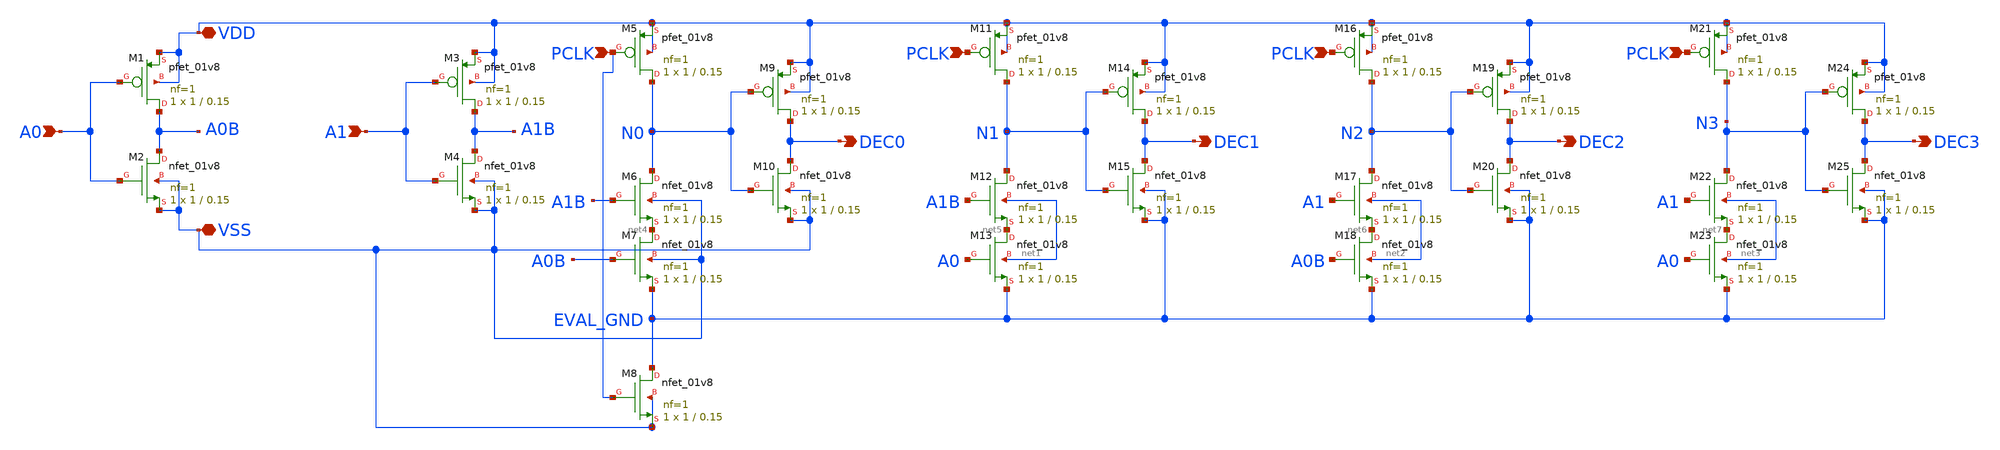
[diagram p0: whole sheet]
** sch_path: cells/row_decoder/row_decoder.sch
**.subckt row_decoder VDD VSS A0 A1 PCLK DEC0 PCLK DEC1 PCLK DEC2 PCLK DEC3
*.iopin VDD
*.iopin VSS
*.ipin A0
*.ipin A1
*.ipin PCLK
*.opin DEC0
*.ipin PCLK
*.opin DEC1
*.ipin PCLK
*.opin DEC2
*.ipin PCLK
*.opin DEC3
XM1 A0B A0 VDD VDD sky130_fd_pr__pfet_01v8 L=0.15 W=1 nf=1 ad='int((nf+1)/2) * W/nf * 0.29' as='int((nf+2)/2) * W/nf * 0.29'
+ pd='2*int((nf+1)/2) * (W/nf + 0.29)' ps='2*int((nf+2)/2) * (W/nf + 0.29)' nrd='0.29 / W' nrs='0.29 / W'
+ sa=0 sb=0 sd=0 mult=1 m=1
XM2 A0B A0 VSS VSS sky130_fd_pr__nfet_01v8 L=0.15 W=1 nf=1 ad='int((nf+1)/2) * W/nf * 0.29' as='int((nf+2)/2) * W/nf * 0.29'
+ pd='2*int((nf+1)/2) * (W/nf + 0.29)' ps='2*int((nf+2)/2) * (W/nf + 0.29)' nrd='0.29 / W' nrs='0.29 / W'
+ sa=0 sb=0 sd=0 mult=1 m=1
XM3 A1B A1 VDD VDD sky130_fd_pr__pfet_01v8 L=0.15 W=1 nf=1 ad='int((nf+1)/2) * W/nf * 0.29' as='int((nf+2)/2) * W/nf * 0.29'
+ pd='2*int((nf+1)/2) * (W/nf + 0.29)' ps='2*int((nf+2)/2) * (W/nf + 0.29)' nrd='0.29 / W' nrs='0.29 / W'
+ sa=0 sb=0 sd=0 mult=1 m=1
XM4 A1B A1 VSS VSS sky130_fd_pr__nfet_01v8 L=0.15 W=1 nf=1 ad='int((nf+1)/2) * W/nf * 0.29' as='int((nf+2)/2) * W/nf * 0.29'
+ pd='2*int((nf+1)/2) * (W/nf + 0.29)' ps='2*int((nf+2)/2) * (W/nf + 0.29)' nrd='0.29 / W' nrs='0.29 / W'
+ sa=0 sb=0 sd=0 mult=1 m=1
XM5 N0 PCLK VDD VDD sky130_fd_pr__pfet_01v8 L=0.15 W=1 nf=1 ad='int((nf+1)/2) * W/nf * 0.29' as='int((nf+2)/2) * W/nf * 0.29'
+ pd='2*int((nf+1)/2) * (W/nf + 0.29)' ps='2*int((nf+2)/2) * (W/nf + 0.29)' nrd='0.29 / W' nrs='0.29 / W'
+ sa=0 sb=0 sd=0 mult=1 m=1
XM6 N0 A1B net4 VSS sky130_fd_pr__nfet_01v8 L=0.15 W=1 nf=1 ad='int((nf+1)/2) * W/nf * 0.29' as='int((nf+2)/2) * W/nf * 0.29'
+ pd='2*int((nf+1)/2) * (W/nf + 0.29)' ps='2*int((nf+2)/2) * (W/nf + 0.29)' nrd='0.29 / W' nrs='0.29 / W'
+ sa=0 sb=0 sd=0 mult=1 m=1
XM7 net4 A0B EVAL_GND VSS sky130_fd_pr__nfet_01v8 L=0.15 W=1 nf=1 ad='int((nf+1)/2) * W/nf * 0.29' as='int((nf+2)/2) * W/nf * 0.29'
+ pd='2*int((nf+1)/2) * (W/nf + 0.29)' ps='2*int((nf+2)/2) * (W/nf + 0.29)' nrd='0.29 / W' nrs='0.29 / W'
+ sa=0 sb=0 sd=0 mult=1 m=1
XM8 EVAL_GND PCLK VSS VSS sky130_fd_pr__nfet_01v8 L=0.15 W=1 nf=1 ad='int((nf+1)/2) * W/nf * 0.29' as='int((nf+2)/2) * W/nf * 0.29'
+ pd='2*int((nf+1)/2) * (W/nf + 0.29)' ps='2*int((nf+2)/2) * (W/nf + 0.29)' nrd='0.29 / W' nrs='0.29 / W'
+ sa=0 sb=0 sd=0 mult=1 m=1
XM9 DEC0 N0 VDD VDD sky130_fd_pr__pfet_01v8 L=0.15 W=1 nf=1 ad='int((nf+1)/2) * W/nf * 0.29' as='int((nf+2)/2) * W/nf * 0.29'
+ pd='2*int((nf+1)/2) * (W/nf + 0.29)' ps='2*int((nf+2)/2) * (W/nf + 0.29)' nrd='0.29 / W' nrs='0.29 / W'
+ sa=0 sb=0 sd=0 mult=1 m=1
XM10 DEC0 N0 VSS VSS sky130_fd_pr__nfet_01v8 L=0.15 W=1 nf=1 ad='int((nf+1)/2) * W/nf * 0.29' as='int((nf+2)/2) * W/nf * 0.29'
+ pd='2*int((nf+1)/2) * (W/nf + 0.29)' ps='2*int((nf+2)/2) * (W/nf + 0.29)' nrd='0.29 / W' nrs='0.29 / W'
+ sa=0 sb=0 sd=0 mult=1 m=1
XM11 N1 PCLK VDD VDD sky130_fd_pr__pfet_01v8 L=0.15 W=1 nf=1 ad='int((nf+1)/2) * W/nf * 0.29' as='int((nf+2)/2) * W/nf * 0.29'
+ pd='2*int((nf+1)/2) * (W/nf + 0.29)' ps='2*int((nf+2)/2) * (W/nf + 0.29)' nrd='0.29 / W' nrs='0.29 / W'
+ sa=0 sb=0 sd=0 mult=1 m=1
XM12 N1 A1B net5 net1 sky130_fd_pr__nfet_01v8 L=0.15 W=1 nf=1 ad='int((nf+1)/2) * W/nf * 0.29' as='int((nf+2)/2) * W/nf * 0.29'
+ pd='2*int((nf+1)/2) * (W/nf + 0.29)' ps='2*int((nf+2)/2) * (W/nf + 0.29)' nrd='0.29 / W' nrs='0.29 / W'
+ sa=0 sb=0 sd=0 mult=1 m=1
XM13 net5 A0 EVAL_GND net1 sky130_fd_pr__nfet_01v8 L=0.15 W=1 nf=1 ad='int((nf+1)/2) * W/nf * 0.29' as='int((nf+2)/2) * W/nf * 0.29'
+ pd='2*int((nf+1)/2) * (W/nf + 0.29)' ps='2*int((nf+2)/2) * (W/nf + 0.29)' nrd='0.29 / W' nrs='0.29 / W'
+ sa=0 sb=0 sd=0 mult=1 m=1
XM14 DEC1 N1 VDD VDD sky130_fd_pr__pfet_01v8 L=0.15 W=1 nf=1 ad='int((nf+1)/2) * W/nf * 0.29' as='int((nf+2)/2) * W/nf * 0.29'
+ pd='2*int((nf+1)/2) * (W/nf + 0.29)' ps='2*int((nf+2)/2) * (W/nf + 0.29)' nrd='0.29 / W' nrs='0.29 / W'
+ sa=0 sb=0 sd=0 mult=1 m=1
XM15 DEC1 N1 EVAL_GND EVAL_GND sky130_fd_pr__nfet_01v8 L=0.15 W=1 nf=1 ad='int((nf+1)/2) * W/nf * 0.29'
+ as='int((nf+2)/2) * W/nf * 0.29' pd='2*int((nf+1)/2) * (W/nf + 0.29)' ps='2*int((nf+2)/2) * (W/nf + 0.29)'
+ nrd='0.29 / W' nrs='0.29 / W' sa=0 sb=0 sd=0 mult=1 m=1
XM16 N2 PCLK VDD VDD sky130_fd_pr__pfet_01v8 L=0.15 W=1 nf=1 ad='int((nf+1)/2) * W/nf * 0.29' as='int((nf+2)/2) * W/nf * 0.29'
+ pd='2*int((nf+1)/2) * (W/nf + 0.29)' ps='2*int((nf+2)/2) * (W/nf + 0.29)' nrd='0.29 / W' nrs='0.29 / W'
+ sa=0 sb=0 sd=0 mult=1 m=1
XM17 N2 A1 net6 net2 sky130_fd_pr__nfet_01v8 L=0.15 W=1 nf=1 ad='int((nf+1)/2) * W/nf * 0.29' as='int((nf+2)/2) * W/nf * 0.29'
+ pd='2*int((nf+1)/2) * (W/nf + 0.29)' ps='2*int((nf+2)/2) * (W/nf + 0.29)' nrd='0.29 / W' nrs='0.29 / W'
+ sa=0 sb=0 sd=0 mult=1 m=1
XM18 net6 A0B EVAL_GND net2 sky130_fd_pr__nfet_01v8 L=0.15 W=1 nf=1 ad='int((nf+1)/2) * W/nf * 0.29'
+ as='int((nf+2)/2) * W/nf * 0.29' pd='2*int((nf+1)/2) * (W/nf + 0.29)' ps='2*int((nf+2)/2) * (W/nf + 0.29)'
+ nrd='0.29 / W' nrs='0.29 / W' sa=0 sb=0 sd=0 mult=1 m=1
XM19 DEC2 N2 VDD VDD sky130_fd_pr__pfet_01v8 L=0.15 W=1 nf=1 ad='int((nf+1)/2) * W/nf * 0.29' as='int((nf+2)/2) * W/nf * 0.29'
+ pd='2*int((nf+1)/2) * (W/nf + 0.29)' ps='2*int((nf+2)/2) * (W/nf + 0.29)' nrd='0.29 / W' nrs='0.29 / W'
+ sa=0 sb=0 sd=0 mult=1 m=1
XM20 DEC2 N2 EVAL_GND EVAL_GND sky130_fd_pr__nfet_01v8 L=0.15 W=1 nf=1 ad='int((nf+1)/2) * W/nf * 0.29'
+ as='int((nf+2)/2) * W/nf * 0.29' pd='2*int((nf+1)/2) * (W/nf + 0.29)' ps='2*int((nf+2)/2) * (W/nf + 0.29)'
+ nrd='0.29 / W' nrs='0.29 / W' sa=0 sb=0 sd=0 mult=1 m=1
XM21 N3 PCLK VDD VDD sky130_fd_pr__pfet_01v8 L=0.15 W=1 nf=1 ad='int((nf+1)/2) * W/nf * 0.29' as='int((nf+2)/2) * W/nf * 0.29'
+ pd='2*int((nf+1)/2) * (W/nf + 0.29)' ps='2*int((nf+2)/2) * (W/nf + 0.29)' nrd='0.29 / W' nrs='0.29 / W'
+ sa=0 sb=0 sd=0 mult=1 m=1
XM22 N3 A1 net7 net3 sky130_fd_pr__nfet_01v8 L=0.15 W=1 nf=1 ad='int((nf+1)/2) * W/nf * 0.29' as='int((nf+2)/2) * W/nf * 0.29'
+ pd='2*int((nf+1)/2) * (W/nf + 0.29)' ps='2*int((nf+2)/2) * (W/nf + 0.29)' nrd='0.29 / W' nrs='0.29 / W'
+ sa=0 sb=0 sd=0 mult=1 m=1
XM23 net7 A0 EVAL_GND net3 sky130_fd_pr__nfet_01v8 L=0.15 W=1 nf=1 ad='int((nf+1)/2) * W/nf * 0.29' as='int((nf+2)/2) * W/nf * 0.29'
+ pd='2*int((nf+1)/2) * (W/nf + 0.29)' ps='2*int((nf+2)/2) * (W/nf + 0.29)' nrd='0.29 / W' nrs='0.29 / W'
+ sa=0 sb=0 sd=0 mult=1 m=1
XM24 DEC3 N3 VDD VDD sky130_fd_pr__pfet_01v8 L=0.15 W=1 nf=1 ad='int((nf+1)/2) * W/nf * 0.29' as='int((nf+2)/2) * W/nf * 0.29'
+ pd='2*int((nf+1)/2) * (W/nf + 0.29)' ps='2*int((nf+2)/2) * (W/nf + 0.29)' nrd='0.29 / W' nrs='0.29 / W'
+ sa=0 sb=0 sd=0 mult=1 m=1
XM25 DEC3 N3 EVAL_GND EVAL_GND sky130_fd_pr__nfet_01v8 L=0.15 W=1 nf=1 ad='int((nf+1)/2) * W/nf * 0.29'
+ as='int((nf+2)/2) * W/nf * 0.29' pd='2*int((nf+1)/2) * (W/nf + 0.29)' ps='2*int((nf+2)/2) * (W/nf + 0.29)'
+ nrd='0.29 / W' nrs='0.29 / W' sa=0 sb=0 sd=0 mult=1 m=1
**.ends
.end
